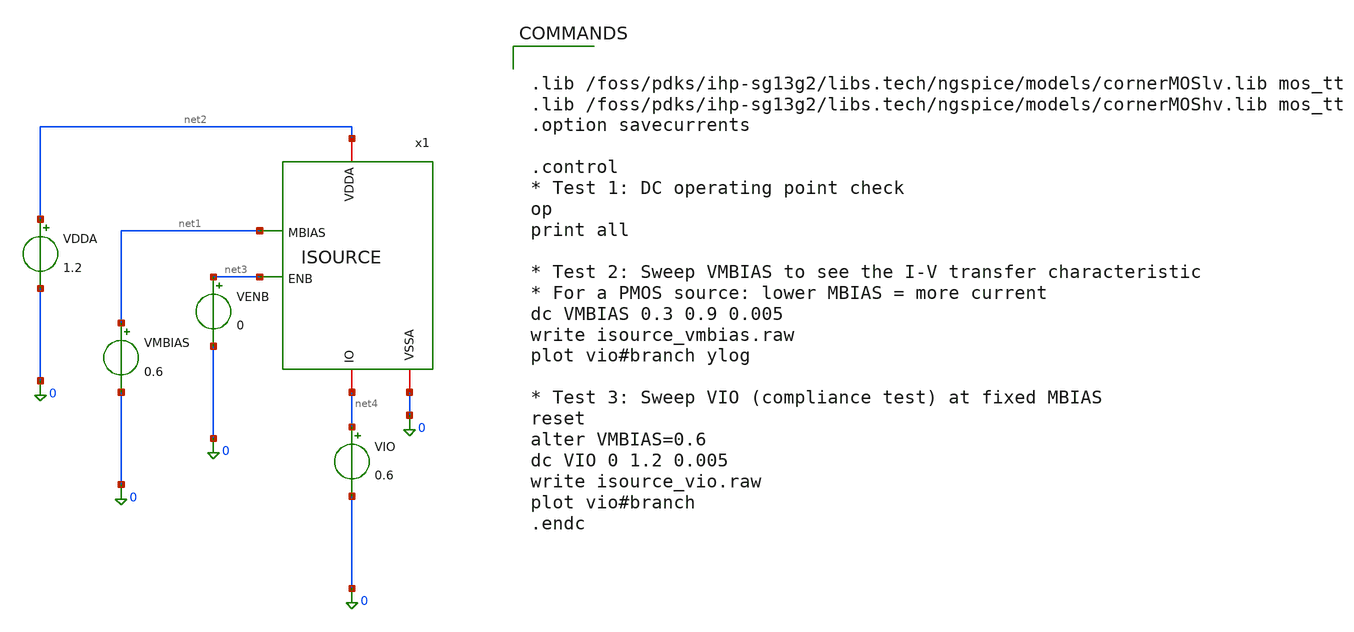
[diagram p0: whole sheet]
** sch_path: ISOURCE_test.sch
**.subckt ISOURCE_test
VMBIAS net1 0 0.6
VDDA net2 0 1.2
VENB net3 0 0
VIO net4 0 0.6
x1 net2 net1 net3 0 net4 ISOURCE
**** begin user architecture code


.lib /foss/pdks/ihp-sg13g2/libs.tech/ngspice/models/cornerMOSlv.lib mos_tt
.lib /foss/pdks/ihp-sg13g2/libs.tech/ngspice/models/cornerMOShv.lib mos_tt
.option savecurrents

.control
* Test 1: DC operating point check
op
print all

* Test 2: Sweep VMBIAS to see the I-V transfer characteristic
* For a PMOS source: lower MBIAS = more current
dc VMBIAS 0.3 0.9 0.005
write isource_vmbias.raw
plot vio#branch ylog

* Test 3: Sweep VIO (compliance test) at fixed MBIAS
reset
alter VMBIAS=0.6
dc VIO 0 1.2 0.005
write isource_vio.raw
plot vio#branch
.endc


**** end user architecture code
**.ends

* expanding   symbol:  ISOURCE.sym # of pins=5
** sym_path: ISOURCE.sym
** sch_path: ISOURCE.sch
.subckt ISOURCE VDDA MBIAS ENB VSSA IO
*.iopin VDDA
*.ipin MBIAS
*.ipin ENB
*.iopin IO
*.iopin VSSA
XM2 net1 MBIAS VDDA VDDA sg13_hv_pmos w=1u l=5u ng=1 m=1 mm_ok=1
XM1 IO ENB net1 VDDA sg13_hv_pmos w=3.3u l=0.5u ng=1 m=1 mm_ok=1
.ends

.end
